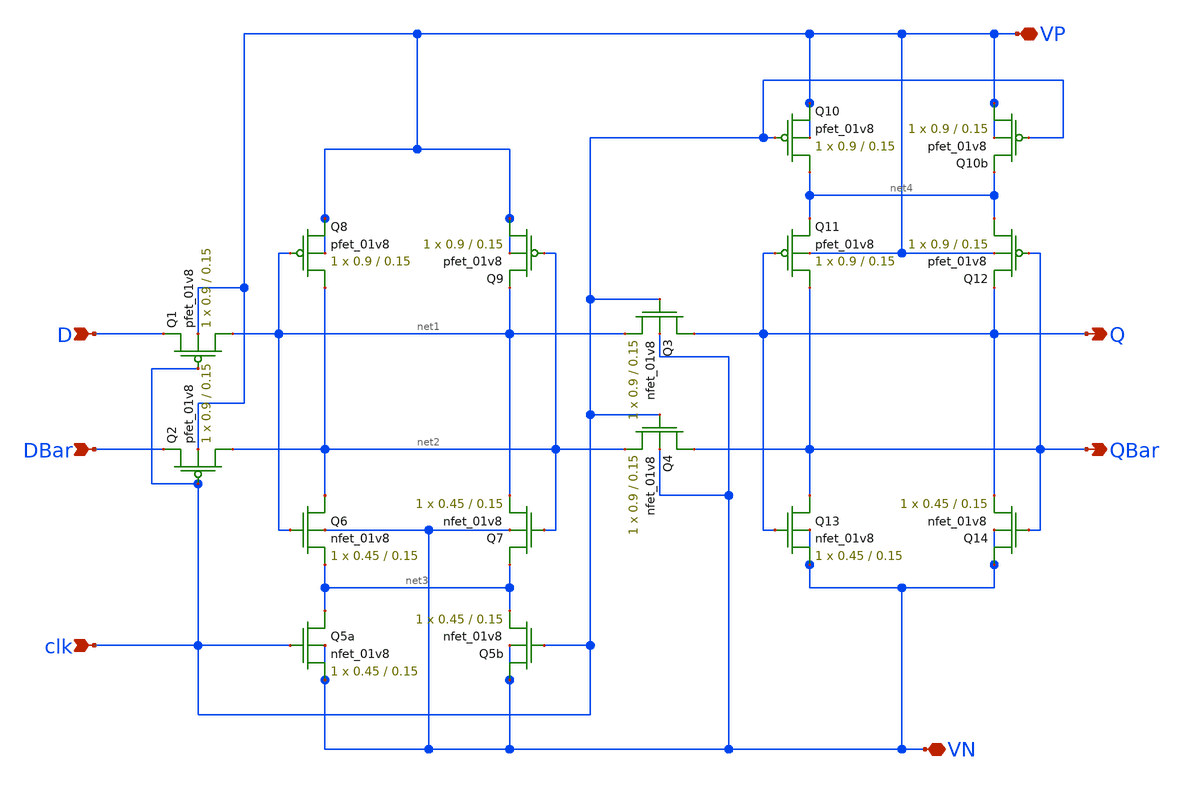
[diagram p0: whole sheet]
** sch_path: MADVLSI_MP2/Sil_CSRL_4_Pin.sch
**.subckt Sil_CSRL_4_Pin VN VP D DBar clk Q QBar
*.iopin VN
*.iopin VP
*.ipin D
*.ipin DBar
*.ipin clk
*.opin Q
*.opin QBar
XQ1 net1 clk D VP sky130_fd_pr__pfet_01v8 L=0.15 W=0.9 nf=1 ad='int((nf+1)/2) * W/nf * 0.29' as='int((nf+2)/2) * W/nf * 0.29'
+ pd='2*int((nf+1)/2) * (W/nf + 0.29)' ps='2*int((nf+2)/2) * (W/nf + 0.29)' nrd='0.29 / W' nrs='0.29 / W'
+ sa=0 sb=0 sd=0 mult=1 m=1
XQ3 Q clk net1 VN sky130_fd_pr__nfet_01v8 L=0.15 W=0.9 nf=1 ad='int((nf+1)/2) * W/nf * 0.29' as='int((nf+2)/2) * W/nf * 0.29'
+ pd='2*int((nf+1)/2) * (W/nf + 0.29)' ps='2*int((nf+2)/2) * (W/nf + 0.29)' nrd='0.29 / W' nrs='0.29 / W'
+ sa=0 sb=0 sd=0 mult=1 m=1
XQ2 net2 clk DBar VP sky130_fd_pr__pfet_01v8 L=0.15 W=0.9 nf=1 ad='int((nf+1)/2) * W/nf * 0.29' as='int((nf+2)/2) * W/nf * 0.29'
+ pd='2*int((nf+1)/2) * (W/nf + 0.29)' ps='2*int((nf+2)/2) * (W/nf + 0.29)' nrd='0.29 / W' nrs='0.29 / W'
+ sa=0 sb=0 sd=0 mult=1 m=1
XQ8 net2 net1 VP VP sky130_fd_pr__pfet_01v8 L=0.15 W=0.9 nf=1 ad='int((nf+1)/2) * W/nf * 0.29' as='int((nf+2)/2) * W/nf * 0.29'
+ pd='2*int((nf+1)/2) * (W/nf + 0.29)' ps='2*int((nf+2)/2) * (W/nf + 0.29)' nrd='0.29 / W' nrs='0.29 / W'
+ sa=0 sb=0 sd=0 mult=1 m=1
XQ9 VP net2 net1 VP sky130_fd_pr__pfet_01v8 L=0.15 W=0.9 nf=1 ad='int((nf+1)/2) * W/nf * 0.29' as='int((nf+2)/2) * W/nf * 0.29'
+ pd='2*int((nf+1)/2) * (W/nf + 0.29)' ps='2*int((nf+2)/2) * (W/nf + 0.29)' nrd='0.29 / W' nrs='0.29 / W'
+ sa=0 sb=0 sd=0 mult=1 m=1
XQ12 net4 QBar Q VP sky130_fd_pr__pfet_01v8 L=0.15 W=0.9 nf=1 ad='int((nf+1)/2) * W/nf * 0.29' as='int((nf+2)/2) * W/nf * 0.29'
+ pd='2*int((nf+1)/2) * (W/nf + 0.29)' ps='2*int((nf+2)/2) * (W/nf + 0.29)' nrd='0.29 / W' nrs='0.29 / W'
+ sa=0 sb=0 sd=0 mult=1 m=1
XQ10 net4 clk VP VP sky130_fd_pr__pfet_01v8 L=0.15 W=0.9 nf=1 ad='int((nf+1)/2) * W/nf * 0.29' as='int((nf+2)/2) * W/nf * 0.29'
+ pd='2*int((nf+1)/2) * (W/nf + 0.29)' ps='2*int((nf+2)/2) * (W/nf + 0.29)' nrd='0.29 / W' nrs='0.29 / W'
+ sa=0 sb=0 sd=0 mult=1 m=1
XQ11 QBar Q net4 VP sky130_fd_pr__pfet_01v8 L=0.15 W=0.9 nf=1 ad='int((nf+1)/2) * W/nf * 0.29' as='int((nf+2)/2) * W/nf * 0.29'
+ pd='2*int((nf+1)/2) * (W/nf + 0.29)' ps='2*int((nf+2)/2) * (W/nf + 0.29)' nrd='0.29 / W' nrs='0.29 / W'
+ sa=0 sb=0 sd=0 mult=1 m=1
XQ4 QBar clk net2 VN sky130_fd_pr__nfet_01v8 L=0.15 W=0.9 nf=1 ad='int((nf+1)/2) * W/nf * 0.29' as='int((nf+2)/2) * W/nf * 0.29'
+ pd='2*int((nf+1)/2) * (W/nf + 0.29)' ps='2*int((nf+2)/2) * (W/nf + 0.29)' nrd='0.29 / W' nrs='0.29 / W'
+ sa=0 sb=0 sd=0 mult=1 m=1
XQ5a net3 clk VN VN sky130_fd_pr__nfet_01v8 L=0.15 W=0.45 nf=1 ad='int((nf+1)/2) * W/nf * 0.29' as='int((nf+2)/2) * W/nf * 0.29'
+ pd='2*int((nf+1)/2) * (W/nf + 0.29)' ps='2*int((nf+2)/2) * (W/nf + 0.29)' nrd='0.29 / W' nrs='0.29 / W'
+ sa=0 sb=0 sd=0 mult=1 m=1
XQ7 net3 net2 net1 VN sky130_fd_pr__nfet_01v8 L=0.15 W=0.45 nf=1 ad='int((nf+1)/2) * W/nf * 0.29' as='int((nf+2)/2) * W/nf * 0.29'
+ pd='2*int((nf+1)/2) * (W/nf + 0.29)' ps='2*int((nf+2)/2) * (W/nf + 0.29)' nrd='0.29 / W' nrs='0.29 / W'
+ sa=0 sb=0 sd=0 mult=1 m=1
XQ6 net2 net1 net3 VN sky130_fd_pr__nfet_01v8 L=0.15 W=0.45 nf=1 ad='int((nf+1)/2) * W/nf * 0.29' as='int((nf+2)/2) * W/nf * 0.29'
+ pd='2*int((nf+1)/2) * (W/nf + 0.29)' ps='2*int((nf+2)/2) * (W/nf + 0.29)' nrd='0.29 / W' nrs='0.29 / W'
+ sa=0 sb=0 sd=0 mult=1 m=1
XQ13 QBar Q VN VN sky130_fd_pr__nfet_01v8 L=0.15 W=0.45 nf=1 ad='int((nf+1)/2) * W/nf * 0.29' as='int((nf+2)/2) * W/nf * 0.29'
+ pd='2*int((nf+1)/2) * (W/nf + 0.29)' ps='2*int((nf+2)/2) * (W/nf + 0.29)' nrd='0.29 / W' nrs='0.29 / W'
+ sa=0 sb=0 sd=0 mult=1 m=1
XQ14 VN QBar Q VN sky130_fd_pr__nfet_01v8 L=0.15 W=0.45 nf=1 ad='int((nf+1)/2) * W/nf * 0.29' as='int((nf+2)/2) * W/nf * 0.29'
+ pd='2*int((nf+1)/2) * (W/nf + 0.29)' ps='2*int((nf+2)/2) * (W/nf + 0.29)' nrd='0.29 / W' nrs='0.29 / W'
+ sa=0 sb=0 sd=0 mult=1 m=1
XQ5b VN clk net3 VN sky130_fd_pr__nfet_01v8 L=0.15 W=0.45 nf=1 ad='int((nf+1)/2) * W/nf * 0.29' as='int((nf+2)/2) * W/nf * 0.29'
+ pd='2*int((nf+1)/2) * (W/nf + 0.29)' ps='2*int((nf+2)/2) * (W/nf + 0.29)' nrd='0.29 / W' nrs='0.29 / W'
+ sa=0 sb=0 sd=0 mult=1 m=1
XQ10b VP clk net4 VP sky130_fd_pr__pfet_01v8 L=0.15 W=0.9 nf=1 ad='int((nf+1)/2) * W/nf * 0.29' as='int((nf+2)/2) * W/nf * 0.29'
+ pd='2*int((nf+1)/2) * (W/nf + 0.29)' ps='2*int((nf+2)/2) * (W/nf + 0.29)' nrd='0.29 / W' nrs='0.29 / W'
+ sa=0 sb=0 sd=0 mult=1 m=1
**.ends
.end
